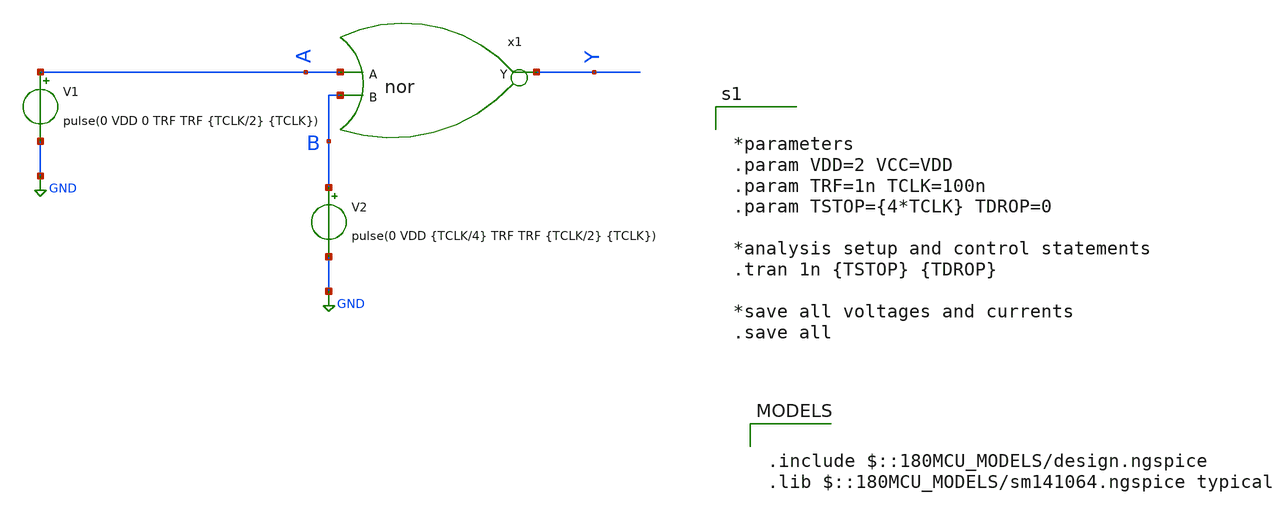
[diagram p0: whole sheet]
** sch_path: XSCHEM Files/nor_tb.sch
**.subckt nor_tb
V1 A GND pulse(0 VDD 0 TRF TRF {TCLK/2} {TCLK})
V2 B GND pulse(0 VDD {TCLK/4} TRF TRF {TCLK/2} {TCLK})
x1 Y A B nor
**** begin user architecture code


*parameters
.param VDD=2 VCC=VDD
.param TRF=1n TCLK=100n
.param TSTOP={4*TCLK} TDROP=0

*analysis setup and control statements
.tran 1n {TSTOP} {TDROP}

*save all voltages and currents
.save all



.include $::180MCU_MODELS/design.ngspice
.lib $::180MCU_MODELS/sm141064.ngspice typical

**** end user architecture code
**.ends

* expanding   symbol:  /home/tare/Desktop/Final/nor.sym # of pins=3
** sym_path: XSCHEM Files/nor.sym
** sch_path: XSCHEM Files/nor.sch
.subckt nor Y A B
*.ipin A
*.opin Y
*.ipin B
**** begin user architecture code


*nor model
a1 [A b] Yi my_nor
.model my_nor d_nor(rise_delay = 1e-9 fall_delay = 1e-9                         input_load = 1e-12)

*force netlisting of digital outputs
v1 Yi Y 0


**** end user architecture code
.ends

.GLOBAL GND
.end
